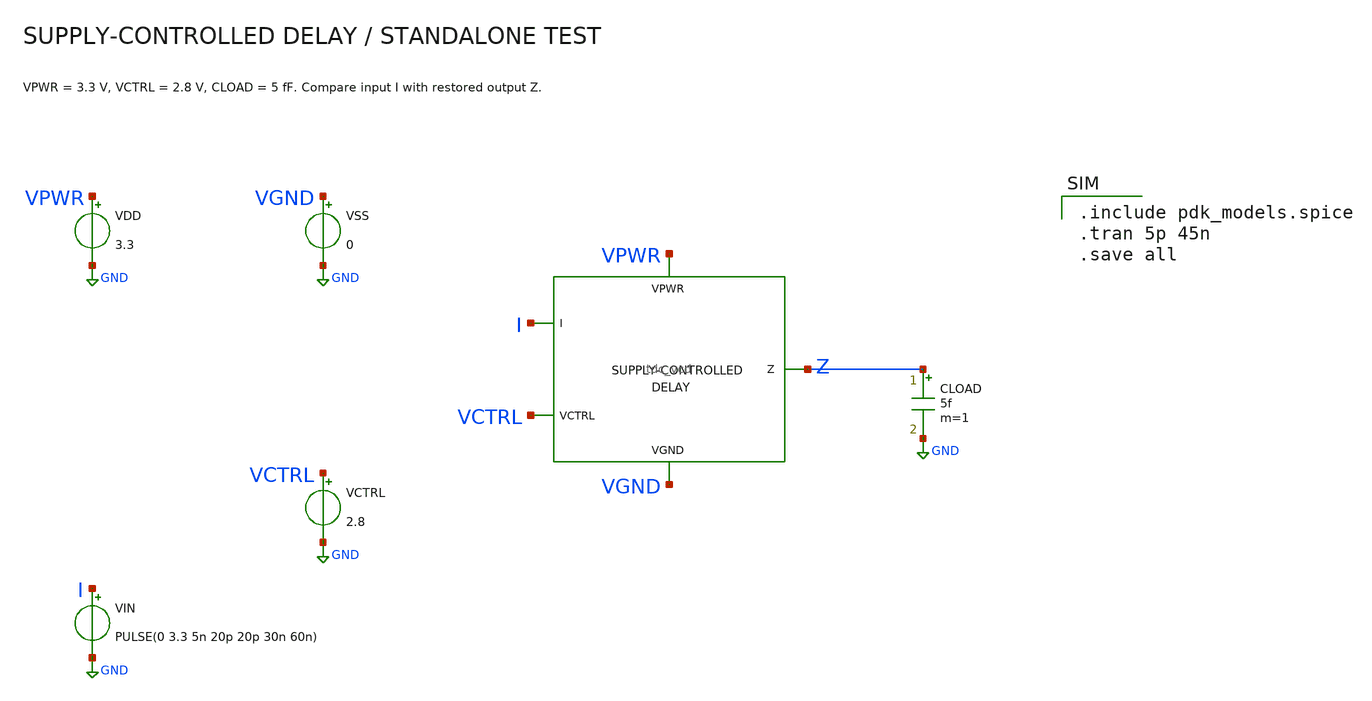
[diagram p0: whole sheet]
** sch_path: schem/tdc_vcd_test.sch
**.subckt tdc_vcd_test
Xdelay I VCTRL Z VPWR VGND tdc_vcd
VDD VPWR GND 3.3
VSS VGND GND 0
VIN I GND PULSE(0 3.3 5n 20p 20p 30n 60n)
VCTRL VCTRL GND 2.8
CLOAD Z GND 5f m=1
**** begin user architecture code

.include pdk_models.spice
.tran 5p 45n
.save all


**** end user architecture code
**.ends

* expanding   symbol:  tdc_vcd.sym # of pins=5
** sym_path: schem/tdc_vcd.sym
** sch_path: schem/tdc_vcd.sch
.subckt tdc_vcd I VCTRL Z VPWR VGND
*.ipin I
*.opin Z
*.iopin VCTRL
*.iopin VPWR
*.iopin VGND
X1 I net1 VCTRL VCTRL VGND VGND gf180mcu_fd_sc_mcu7t5v0__dlya_1
X2 net1 net2 VCTRL VCTRL VGND VGND gf180mcu_fd_sc_mcu7t5v0__dlya_1
X3 net2 Z VPWR VPWR VGND VGND gf180mcu_fd_sc_mcu7t5v0__buf_4
.ends

.GLOBAL GND
.end
